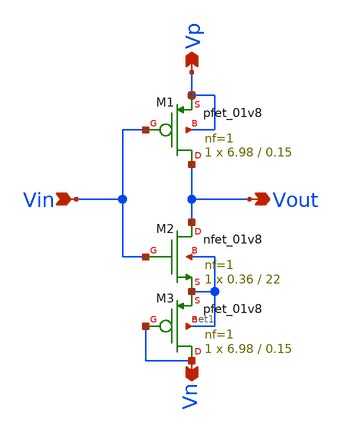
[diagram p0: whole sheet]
** sch_path: xschem/Vth_sch/Symbol/Inverter-th13.sch
**.subckt Inverter-th13 Vin Vout Vp Vn
*.ipin Vin
*.opin Vout
*.opin Vp
*.opin Vn
XM1 Vout Vin Vp Vp sky130_fd_pr__pfet_01v8 L=0.15 W=6.98 nf=1 ad='int((nf+1)/2) * W/nf * 0.29' as='int((nf+2)/2) * W/nf * 0.29'
+ pd='2*int((nf+1)/2) * (W/nf + 0.29)' ps='2*int((nf+2)/2) * (W/nf + 0.29)' nrd='0.29 / W' nrs='0.29 / W'
+ sa=0 sb=0 sd=0 mult=1 m=1
XM2 Vout Vin net1 net1 sky130_fd_pr__nfet_01v8 L=22 W=0.36 nf=1 ad='int((nf+1)/2) * W/nf * 0.29' as='int((nf+2)/2) * W/nf * 0.29'
+ pd='2*int((nf+1)/2) * (W/nf + 0.29)' ps='2*int((nf+2)/2) * (W/nf + 0.29)' nrd='0.29 / W' nrs='0.29 / W'
+ sa=0 sb=0 sd=0 mult=1 m=1
XM3 Vn Vn net1 net1 sky130_fd_pr__pfet_01v8 L=0.15 W=6.98 nf=1 ad='int((nf+1)/2) * W/nf * 0.29' as='int((nf+2)/2) * W/nf * 0.29'
+ pd='2*int((nf+1)/2) * (W/nf + 0.29)' ps='2*int((nf+2)/2) * (W/nf + 0.29)' nrd='0.29 / W' nrs='0.29 / W'
+ sa=0 sb=0 sd=0 mult=1 m=1
**.ends
.end
